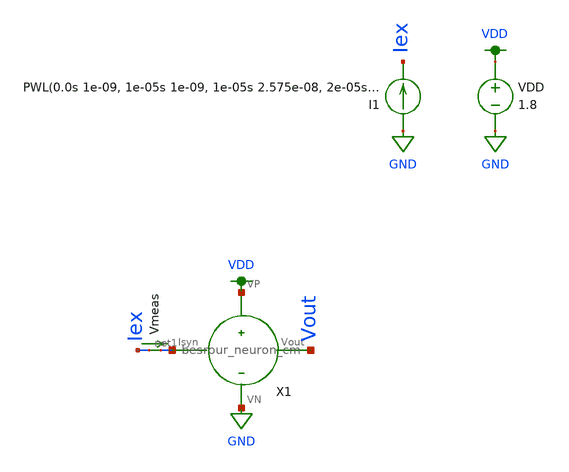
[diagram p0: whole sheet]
** sch_path: schematic/tran_besrour_neuron.sch
**.subckt tran_besrour_neuron
X1 net1 Vout VDD GND besrour_neuron_cm
VDD VDD GND 1.8
I1 GND Iex PWL(0.0s 1e-09, 1e-05s 1e-09, 1e-05s 2.575e-08, 2e-05s 2.575e-08, 2e-05s 5.05e-08, 3e-05s
+ 5.05e-08, 3e-05s 7.525e-08, 4e-05s 7.525e-08, 4e-05s 1e-07, 5e-05s 1e-07, 5e-05s 1.9e-07, 6e-05s 1.9e-07,
+ 6e-05s 2.8e-07, 7e-05s 2.8e-07, 7e-05s 3.7e-07, 8e-05s 3.7e-07, 8e-05s 4.6e-07, 9e-05s 4.6e-07, 9e-05s
+ 5.5e-07, 0.0001s 5.5e-07, 0.0001s 6.4e-07, 0.00011s 6.4e-07, 0.00011s 7.3e-07, 0.00012s 7.3e-07, 0.00012s
+ 8.2e-07, 0.00013s 8.2e-07, 0.00013s 9.1e-07, 0.00014s 9.1e-07, 0.00014s 1e-06, 0.00015s 1e-06, 0.00015s
+ 2.8e-06, 0.00016s 2.8e-06, 0.00016s 4.6e-06, 0.00017s 4.6e-06, 0.00017s 6.4e-06, 0.00018s 6.4e-06, 0.00018s
+ 8.2e-06, 0.00019s 8.2e-06, 0.00019s 1e-05, 0.0002s 1e-05, 0.0002s 2.267e-05, 0.00021s 2.267e-05, 0.00021s
+ 3.533e-05, 0.00022s 3.533e-05, 0.00022s 4.8e-05, 0.00023s 4.8e-05, 0.00023s 6.067e-05, 0.00024s 6.067e-05,
+ 0.00024s 7.333e-05, 0.00025s 7.333e-05, 0.00025s 8.6e-05, 0.00026s 8.6e-05, 0.00026s 9.867e-05, 0.00027s
+ 9.867e-05, 0.00027s 0.000111333, 0.00028s 0.000111333, 0.00028s 0.000124, 0.00029s 0.000124, 0.00029s
+ 0.000136667, 0.0003s 0.000136667, 0.0003s 0.000149333, 0.00031s 0.000149333, 0.00031s 0.000162, 0.00032s
+ 0.000162, 0.00032s 0.000174667, 0.00033s 0.000174667, 0.00033s 0.000187333, 0.00034s 0.000187333, 0.00034s
+ 0.0002, 0.00035s 0.0002)

Vmeas Iex net1 0
.save i(vmeas)
**** begin user architecture code

.param W=2
.param L=0.3
.control
set wr_vecnames
set wr_singlescale
save all
tran 1ns 350us
wrdata ~/neuromorphic_computing_final/simulation/besrour/mem.txt i(Vmeas) v(Vout)
set appendwrite
.endc



.option wnflag=1
.param MC_SWITCH=0.0
.lib ~/skywater/skywater-pdk/libraries/sky130_fd_pr_ngspice/latest/models/sky130.lib.spice tt

**** end user architecture code
**.ends

* expanding   symbol:  /home/madvlsi/neuromorphic_computing_final/schematic/besrour_neuron_cm.sym #
*+ of pins=4
** sym_path: schematic/besrour_neuron_cm.sym
** sch_path: schematic/besrour_neuron_cm.sch
.subckt besrour_neuron_cm Isyn Vout VP VN
*.iopin VP
*.iopin VN
*.iopin Isyn
*.opin Vout
XM2 VMEMINT net1 VP VDD sky130_fd_pr__pfet_01v8 L={L} W={W} nf=1 ad='int((nf+1)/2) * W/nf * 0.29' as='int((nf+2)/2) * W/nf * 0.29'
+ pd='2*int((nf+1)/2) * (W/nf + 0.29)' ps='2*int((nf+2)/2) * (W/nf + 0.29)' nrd='0.29 / W' nrs='0.29 / W'
+ sa=0 sb=0 sd=0 mult=1 m=1
XM3 VP net3 VMEMINT VDD sky130_fd_pr__pfet_01v8 L={L} W={W} nf=1 ad='int((nf+1)/2) * W/nf * 0.29' as='int((nf+2)/2) * W/nf * 0.29'
+ pd='2*int((nf+1)/2) * (W/nf + 0.29)' ps='2*int((nf+2)/2) * (W/nf + 0.29)' nrd='0.29 / W' nrs='0.29 / W'
+ sa=0 sb=0 sd=0 mult=1 m=1
XM4 net3 VMEMINT VP VDD sky130_fd_pr__pfet_01v8 L={L} W={W} nf=1 ad='int((nf+1)/2) * W/nf * 0.29' as='int((nf+2)/2) * W/nf * 0.29'
+ pd='2*int((nf+1)/2) * (W/nf + 0.29)' ps='2*int((nf+2)/2) * (W/nf + 0.29)' nrd='0.29 / W' nrs='0.29 / W'
+ sa=0 sb=0 sd=0 mult=1 m=1
XM5 net2 net3 VP VDD sky130_fd_pr__pfet_01v8 L={L} W={W} nf=1 ad='int((nf+1)/2) * W/nf * 0.29' as='int((nf+2)/2) * W/nf * 0.29'
+ pd='2*int((nf+1)/2) * (W/nf + 0.29)' ps='2*int((nf+2)/2) * (W/nf + 0.29)' nrd='0.29 / W' nrs='0.29 / W'
+ sa=0 sb=0 sd=0 mult=1 m=1
XM6 net3 VMEMINT VN GND sky130_fd_pr__nfet_01v8 L={L} W={W} nf=1 ad='int((nf+1)/2) * W/nf * 0.29' as='int((nf+2)/2) * W/nf * 0.29'
+ pd='2*int((nf+1)/2) * (W/nf + 0.29)' ps='2*int((nf+2)/2) * (W/nf + 0.29)' nrd='0.29 / W' nrs='0.29 / W'
+ sa=0 sb=0 sd=0 mult=1 m=1
XM8 net2 net3 VN GND sky130_fd_pr__nfet_01v8 L={L} W={W} nf=1 ad='int((nf+1)/2) * W/nf * 0.29' as='int((nf+2)/2) * W/nf * 0.29'
+ pd='2*int((nf+1)/2) * (W/nf + 0.29)' ps='2*int((nf+2)/2) * (W/nf + 0.29)' nrd='0.29 / W' nrs='0.29 / W'
+ sa=0 sb=0 sd=0 mult=1 m=1
C1 VMEMINT VN 340f m=1
C2 net2 VN 340f m=1
XM9 net4 net2 VP VDD sky130_fd_pr__pfet_01v8 L={L} W={W} nf=1 ad='int((nf+1)/2) * W/nf * 0.29' as='int((nf+2)/2) * W/nf * 0.29'
+ pd='2*int((nf+1)/2) * (W/nf + 0.29)' ps='2*int((nf+2)/2) * (W/nf + 0.29)' nrd='0.29 / W' nrs='0.29 / W'
+ sa=0 sb=0 sd=0 mult=1 m=1
XM10 net4 net2 VN GND sky130_fd_pr__nfet_01v8 L={L} W={W} nf=1 ad='int((nf+1)/2) * W/nf * 0.29' as='int((nf+2)/2) * W/nf * 0.29'
+ pd='2*int((nf+1)/2) * (W/nf + 0.29)' ps='2*int((nf+2)/2) * (W/nf + 0.29)' nrd='0.29 / W' nrs='0.29 / W'
+ sa=0 sb=0 sd=0 mult=1 m=1
XM11 Vout net4 VP VDD sky130_fd_pr__pfet_01v8 L={L} W={W} nf=1 ad='int((nf+1)/2) * W/nf * 0.29' as='int((nf+2)/2) * W/nf * 0.29'
+ pd='2*int((nf+1)/2) * (W/nf + 0.29)' ps='2*int((nf+2)/2) * (W/nf + 0.29)' nrd='0.29 / W' nrs='0.29 / W'
+ sa=0 sb=0 sd=0 mult=1 m=1
XM12 Vout net4 VN GND sky130_fd_pr__nfet_01v8 L={L} W={W} nf=1 ad='int((nf+1)/2) * W/nf * 0.29' as='int((nf+2)/2) * W/nf * 0.29'
+ pd='2*int((nf+1)/2) * (W/nf + 0.29)' ps='2*int((nf+2)/2) * (W/nf + 0.29)' nrd='0.29 / W' nrs='0.29 / W'
+ sa=0 sb=0 sd=0 mult=1 m=1
XM13 net1 Isyn VN GND sky130_fd_pr__nfet_01v8 L={L} W={W} nf=1 ad='int((nf+1)/2) * W/nf * 0.29' as='int((nf+2)/2) * W/nf * 0.29'
+ pd='2*int((nf+1)/2) * (W/nf + 0.29)' ps='2*int((nf+2)/2) * (W/nf + 0.29)' nrd='0.29 / W' nrs='0.29 / W'
+ sa=0 sb=0 sd=0 mult=1 m=1
XM14 VN Isyn Isyn GND sky130_fd_pr__nfet_01v8 L={L} W={W} nf=1 ad='int((nf+1)/2) * W/nf * 0.29' as='int((nf+2)/2) * W/nf * 0.29'
+ pd='2*int((nf+1)/2) * (W/nf + 0.29)' ps='2*int((nf+2)/2) * (W/nf + 0.29)' nrd='0.29 / W' nrs='0.29 / W'
+ sa=0 sb=0 sd=0 mult=1 m=1
XM1 VP net1 net1 VDD sky130_fd_pr__pfet_01v8 L={L} W={W} nf=1 ad='int((nf+1)/2) * W/nf * 0.29' as='int((nf+2)/2) * W/nf * 0.29'
+ pd='2*int((nf+1)/2) * (W/nf + 0.29)' ps='2*int((nf+2)/2) * (W/nf + 0.29)' nrd='0.29 / W' nrs='0.29 / W'
+ sa=0 sb=0 sd=0 mult=1 m=1
XM7 VN net2 VMEMINT GND sky130_fd_pr__nfet_01v8 L={L} W={W} nf=1 ad='int((nf+1)/2) * W/nf * 0.29' as='int((nf+2)/2) * W/nf * 0.29'
+ pd='2*int((nf+1)/2) * (W/nf + 0.29)' ps='2*int((nf+2)/2) * (W/nf + 0.29)' nrd='0.29 / W' nrs='0.29 / W'
+ sa=0 sb=0 sd=0 mult=1 m=1
.ends

.GLOBAL GND
.GLOBAL VDD
.end
